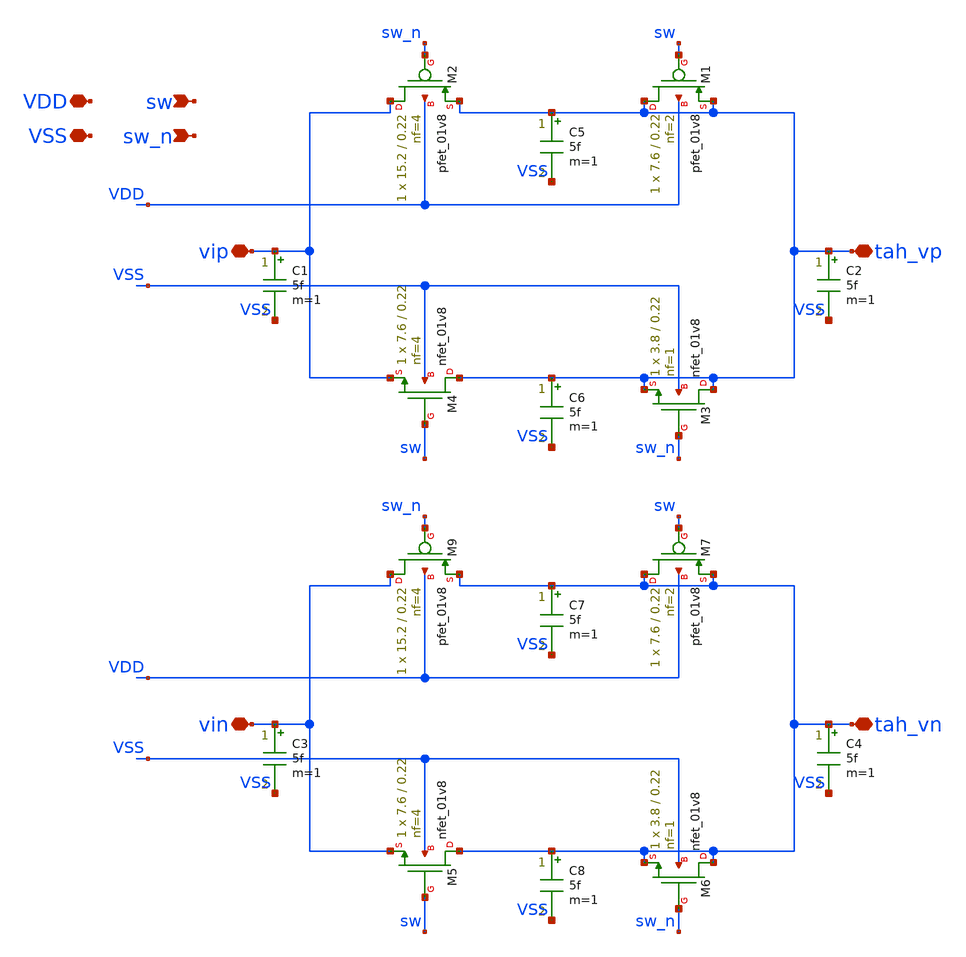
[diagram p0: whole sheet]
** sch_path: hgu/xschem/hgu_tah.sch
**.subckt hgu_tah tah_vp vip VDD VSS sw sw_n tah_vn vin
*.iopin tah_vp
*.iopin vip
*.iopin VDD
*.iopin VSS
*.ipin sw
*.ipin sw_n
*.iopin tah_vn
*.iopin vin
XM1 tah_vp sw tah_vp VDD sky130_fd_pr__pfet_01v8 L=0.22 W=7.6 nf=2 ad='int((nf+1)/2) * W/nf * 0.29' as='int((nf+2)/2) * W/nf * 0.29'
+ pd='2*int((nf+1)/2) * (W/nf + 0.29)' ps='2*int((nf+2)/2) * (W/nf + 0.29)' nrd='0.29 / W' nrs='0.29 / W'
+ sa=0 sb=0 sd=0 mult=1 m=1
XM4 tah_vp sw vip VSS sky130_fd_pr__nfet_01v8 L=0.22 W=7.6 nf=4 ad='int((nf+1)/2) * W/nf * 0.29' as='int((nf+2)/2) * W/nf * 0.29'
+ pd='2*int((nf+1)/2) * (W/nf + 0.29)' ps='2*int((nf+2)/2) * (W/nf + 0.29)' nrd='0.29 / W' nrs='0.29 / W'
+ sa=0 sb=0 sd=0 mult=1 m=1
XM2 vip sw_n tah_vp VDD sky130_fd_pr__pfet_01v8 L=0.22 W=15.2 nf=4 ad='int((nf+1)/2) * W/nf * 0.29' as='int((nf+2)/2) * W/nf * 0.29'
+ pd='2*int((nf+1)/2) * (W/nf + 0.29)' ps='2*int((nf+2)/2) * (W/nf + 0.29)' nrd='0.29 / W' nrs='0.29 / W'
+ sa=0 sb=0 sd=0 mult=1 m=1
XM3 tah_vp sw_n tah_vp VSS sky130_fd_pr__nfet_01v8 L=0.22 W=3.8 nf=1 ad='int((nf+1)/2) * W/nf * 0.29'
+ as='int((nf+2)/2) * W/nf * 0.29' pd='2*int((nf+1)/2) * (W/nf + 0.29)' ps='2*int((nf+2)/2) * (W/nf + 0.29)'
+ nrd='0.29 / W' nrs='0.29 / W' sa=0 sb=0 sd=0 mult=1 m=1
XM9 vin sw_n tah_vn VDD sky130_fd_pr__pfet_01v8 L=0.22 W=15.2 nf=4 ad='int((nf+1)/2) * W/nf * 0.29' as='int((nf+2)/2) * W/nf * 0.29'
+ pd='2*int((nf+1)/2) * (W/nf + 0.29)' ps='2*int((nf+2)/2) * (W/nf + 0.29)' nrd='0.29 / W' nrs='0.29 / W'
+ sa=0 sb=0 sd=0 mult=1 m=1
XM7 tah_vn sw tah_vn VDD sky130_fd_pr__pfet_01v8 L=0.22 W=7.6 nf=2 ad='int((nf+1)/2) * W/nf * 0.29' as='int((nf+2)/2) * W/nf * 0.29'
+ pd='2*int((nf+1)/2) * (W/nf + 0.29)' ps='2*int((nf+2)/2) * (W/nf + 0.29)' nrd='0.29 / W' nrs='0.29 / W'
+ sa=0 sb=0 sd=0 mult=1 m=1
XM5 tah_vn sw vin VSS sky130_fd_pr__nfet_01v8 L=0.22 W=7.6 nf=4 ad='int((nf+1)/2) * W/nf * 0.29' as='int((nf+2)/2) * W/nf * 0.29'
+ pd='2*int((nf+1)/2) * (W/nf + 0.29)' ps='2*int((nf+2)/2) * (W/nf + 0.29)' nrd='0.29 / W' nrs='0.29 / W'
+ sa=0 sb=0 sd=0 mult=1 m=1
XM6 tah_vn sw_n tah_vn VSS sky130_fd_pr__nfet_01v8 L=0.22 W=3.8 nf=1 ad='int((nf+1)/2) * W/nf * 0.29'
+ as='int((nf+2)/2) * W/nf * 0.29' pd='2*int((nf+1)/2) * (W/nf + 0.29)' ps='2*int((nf+2)/2) * (W/nf + 0.29)'
+ nrd='0.29 / W' nrs='0.29 / W' sa=0 sb=0 sd=0 mult=1 m=1
C1 vip VSS 5f m=1
C2 tah_vp VSS 5f m=1
C3 vin VSS 5f m=1
C4 tah_vn VSS 5f m=1
C5 tah_vp VSS 5f m=1
C6 tah_vp VSS 5f m=1
C7 tah_vn VSS 5f m=1
C8 tah_vn VSS 5f m=1
**.ends
.end
